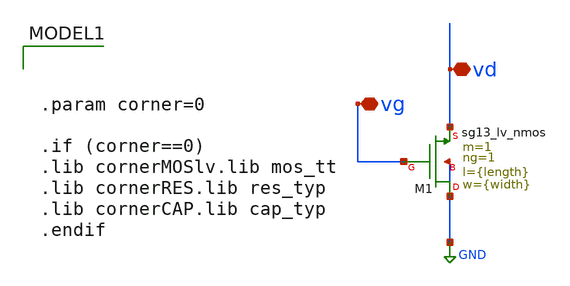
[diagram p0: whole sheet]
** sch_path: Tarea_1/xschem/Length_sweep.sch
**.subckt Length_sweep vg vd
*.iopin vg
*.iopin vd
XM1 GND vg vd GND sg13_lv_nmos w={width} l={length} ng=1 m=1 mm_ok=1
**** begin user architecture code


.param corner=0

.if (corner==0)
.lib cornerMOSlv.lib mos_tt
.lib cornerRES.lib res_typ
.lib cornerCAP.lib cap_typ
.endif



.option wnflag=1
*vsup VDD 0 1.8
vin vg 0 dc=0.45 ac=1
vds vd 0 1.8
.param length = 0.13u
.param width = 0.3u
cload vd 0 5p
*.dc vin 0.0 1.8 0.01

.control
let strt_l = 0.13u
let stop_l = 1.13u
let step_l = 0.01u
let curr_l = strt_l

shell rm -f ao_sweep_l.raw

while curr_l le stop_l
    alterparam length = $&curr_l
    reset
    save all
    save @n.xm1.nsg13_lv_nmos[gm]
    save @n.xm1.nsg13_lv_nmos[gds]
    dc vds 0.02 1.8 0.01

    let gm = @n.xm1.nsg13_lv_nmos[gm]
    let gds = @n.xm1.nsg13_lv_nmos[gds]

    let ao = gm / gds
    *print ao

    set appendwrite
    wrdata ao_sweep_l.raw ao

    let curr_l = curr_l + step_l
end
.endc



**** end user architecture code
**.ends
.GLOBAL GND
.end
